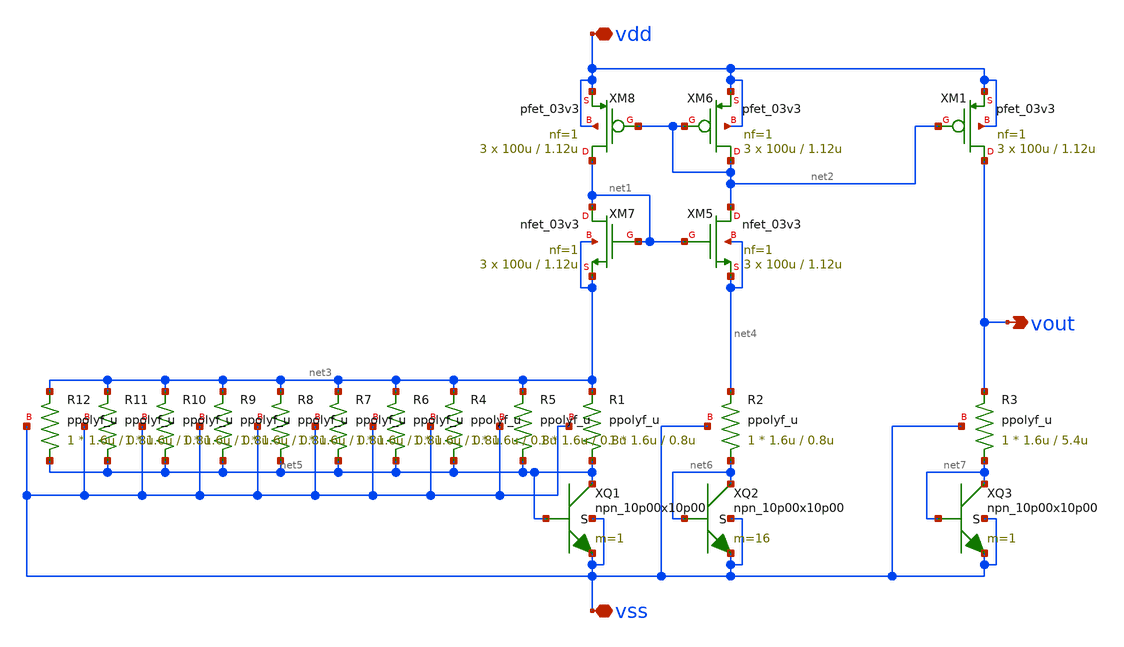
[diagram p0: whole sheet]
** sch_path: maple0705/SAR_ADC/xschem/bgr_diode.sch
**.subckt bgr_diode vdd vss vout
*.iopin vdd
*.iopin vss
*.opin vout
XM5 net2 net1 net4 net4 nfet_03v3 L=1.12u W=100u nf=1 ad='int((nf+1)/2) * W/nf * 0.18u' as='int((nf+2)/2) * W/nf * 0.18u'
+ pd='2*int((nf+1)/2) * (W/nf + 0.18u)' ps='2*int((nf+2)/2) * (W/nf + 0.18u)' nrd='0.18u / W' nrs='0.18u / W'
+ sa=0 sb=0 sd=0 m=3
XM6 net2 net2 vdd vdd pfet_03v3 L=1.12u W=100u nf=1 ad='int((nf+1)/2) * W/nf * 0.18u' as='int((nf+2)/2) * W/nf * 0.18u'
+ pd='2*int((nf+1)/2) * (W/nf + 0.18u)' ps='2*int((nf+2)/2) * (W/nf + 0.18u)' nrd='0.18u / W' nrs='0.18u / W'
+ sa=0 sb=0 sd=0 m=3
XM7 net1 net1 net3 net3 nfet_03v3 L=1.12u W=100u nf=1 ad='int((nf+1)/2) * W/nf * 0.18u' as='int((nf+2)/2) * W/nf * 0.18u'
+ pd='2*int((nf+1)/2) * (W/nf + 0.18u)' ps='2*int((nf+2)/2) * (W/nf + 0.18u)' nrd='0.18u / W' nrs='0.18u / W'
+ sa=0 sb=0 sd=0 m=3
XM8 net1 net2 vdd vdd pfet_03v3 L=1.12u W=100u nf=1 ad='int((nf+1)/2) * W/nf * 0.18u' as='int((nf+2)/2) * W/nf * 0.18u'
+ pd='2*int((nf+1)/2) * (W/nf + 0.18u)' ps='2*int((nf+2)/2) * (W/nf + 0.18u)' nrd='0.18u / W' nrs='0.18u / W'
+ sa=0 sb=0 sd=0 m=3
XQ1 net5 net5 vss vss npn_10p00x10p00 m=1
XQ2 net6 net6 vss vss npn_10p00x10p00 m=16
XM1 vout net2 vdd vdd pfet_03v3 L=1.12u W=100u nf=1 ad='int((nf+1)/2) * W/nf * 0.18u' as='int((nf+2)/2) * W/nf * 0.18u'
+ pd='2*int((nf+1)/2) * (W/nf + 0.18u)' ps='2*int((nf+2)/2) * (W/nf + 0.18u)' nrd='0.18u / W' nrs='0.18u / W'
+ sa=0 sb=0 sd=0 m=3
XQ3 net7 net7 vss vss npn_10p00x10p00 m=1
XR1 net5 net3 vss ppolyf_u r_width=1.6u r_length=0.8u m=1
XR2 net6 net4 vss ppolyf_u r_width=1.6u r_length=0.8u m=1
XR3 net7 vout vss ppolyf_u r_width=1.6u r_length=5.4u m=1
XR4 net5 net3 vss ppolyf_u r_width=1.6u r_length=0.8u m=1
XR5 net5 net3 vss ppolyf_u r_width=1.6u r_length=0.8u m=1
XR6 net5 net3 vss ppolyf_u r_width=1.6u r_length=0.8u m=1
XR7 net5 net3 vss ppolyf_u r_width=1.6u r_length=0.8u m=1
XR8 net5 net3 vss ppolyf_u r_width=1.6u r_length=0.8u m=1
XR9 net5 net3 vss ppolyf_u r_width=1.6u r_length=0.8u m=1
XR10 net5 net3 vss ppolyf_u r_width=1.6u r_length=0.8u m=1
XR11 net5 net3 vss ppolyf_u r_width=1.6u r_length=0.8u m=1
XR12 net5 net3 vss ppolyf_u r_width=1.6u r_length=0.8u m=1
**.ends
.end
